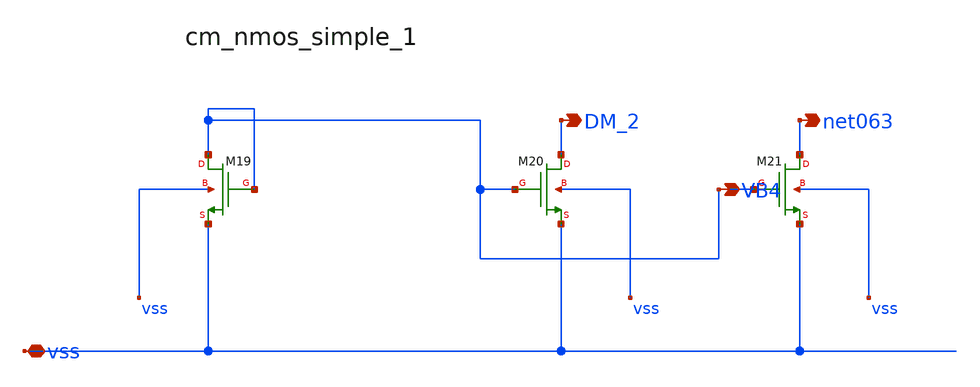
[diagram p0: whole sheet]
** sch_path: analog-db/raw/amp_021_yan_az/hier/blocks/cm_nmos_simple_1.sch
**.subckt cm_nmos_simple_1 vss VB4 DM_2 net063
*.iopin vss
*.opin VB4
*.opin DM_2
*.opin net063
XM19 VB4 VB4 vss vss sg13_lv_nmos w=x_dut_xm19_w l=x_dut_xm19_l ng=1 m=x_dut_xm19_m
XM20 DM_2 VB4 vss vss sg13_lv_nmos w=x_dut_xm20_w l=x_dut_xm20_l ng=1 m=x_dut_xm20_m
XM21 net063 VB4 vss vss sg13_lv_nmos w=x_dut_xm21_w l=x_dut_xm21_l ng=1 m=x_dut_xm21_m
**.ends
.end
